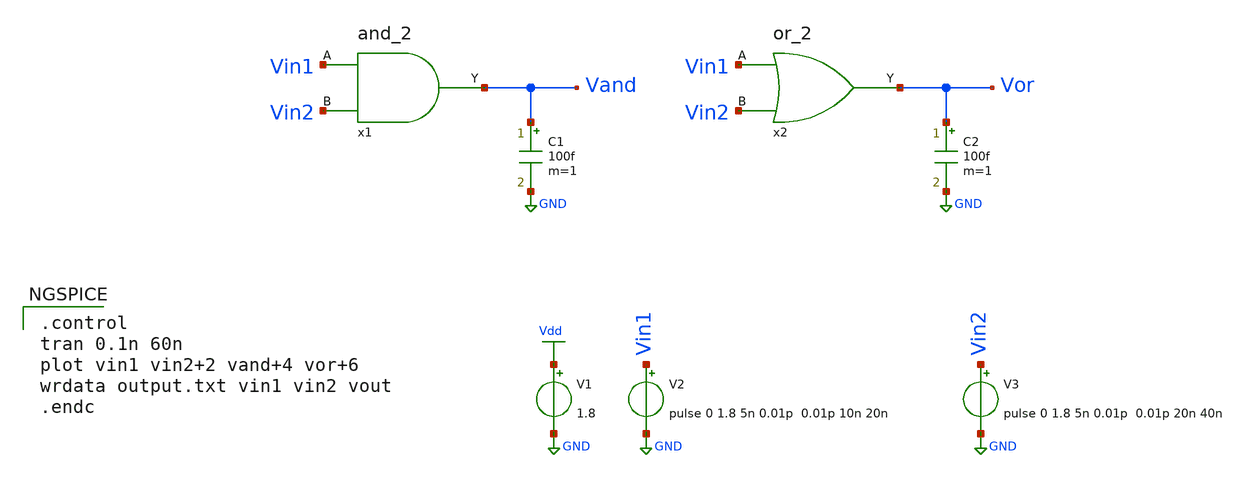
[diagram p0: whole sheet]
** sch_path: Circuiti/porta-nor.sch
**.subckt porta-nor
V1 Vdd GND 1.8
V2 Vin1 GND pulse 0 1.8 5n 0.01p 0.01p 10n 20n
C1 Vand GND 100f m=1
V3 Vin2 GND pulse 0 1.8 5n 0.01p 0.01p 20n 40n
x1 Vin1 Vand Vin2 and_2
C2 Vor GND 100f m=1
x2 Vin1 Vor Vin2 or_2
**** begin user architecture code


.lib /home/matteo/xschem_downloads/skywater-pdk/libraries/sky130_fd_pr_ngspice/latest/models/sky130.lib.spice tt

*.include /home/matteo/xschem_downloads/skywater-pdk/libraries/sky130_fd_pr_ngspice/latest/cells/nfet_01v8/sky130_fd_pr__nfet_01v8__tt.corner.spice

.param mc_mm_switch=0
.param mc_pr_switch=1



.control
tran 0.1n 60n
plot vin1 vin2+2 vand+4 vor+6
wrdata output.txt vin1 vin2 vout
.endc


**** end user architecture code
**.ends

* expanding   symbol:  /home/matteo/Documenti/tesi/Circuiti/logic_gates_sch_sym/and_2.sym # of
*+ pins=3
** sym_path: Circuiti/logic_gates_sch_sym/and_2.sym
** sch_path: Circuiti/logic_gates_sch_sym/and_2.sch
.subckt and_2 A Y B
*.ipin B
*.ipin A
*.opin Y
x1 A net1 B nand_2
x2 net1 Y not
.ends


* expanding   symbol:  /home/matteo/Documenti/tesi/Circuiti/logic_gates_sch_sym/or_2.sym # of pins=3
** sym_path: Circuiti/logic_gates_sch_sym/or_2.sym
** sch_path: Circuiti/logic_gates_sch_sym/or_2.sch
.subckt or_2 A Y B
*.ipin A
*.ipin B
*.opin Y
x1 A net1 B nor_2
x2 net1 Y not
.ends


* expanding   symbol:  /home/matteo/Documenti/tesi/Circuiti/logic_gates_sch_sym/nand_2.sym # of
*+ pins=3
** sym_path: Circuiti/logic_gates_sch_sym/nand_2.sym
** sch_path: Circuiti/logic_gates_sch_sym/nand_2.sch
.subckt nand_2 A Y B
*.ipin A
*.ipin B
*.opin Y
XM1 Y A net1 GND sky130_fd_pr__nfet_01v8 L=0.15 W=1 nf=1 ad='int((nf+1)/2) * W/nf * 0.29' as='int((nf+2)/2) * W/nf * 0.29'
+ pd='2*int((nf+1)/2) * (W/nf + 0.29)' ps='2*int((nf+2)/2) * (W/nf + 0.29)' nrd='0.29 / W' nrs='0.29 / W'
+ sa=0 sb=0 sd=0 mult=1 m=1
XM3 Y B Vdd VDD sky130_fd_pr__pfet_01v8 L=0.45 W=4.8 nf=1 ad='int((nf+1)/2) * W/nf * 0.29' as='int((nf+2)/2) * W/nf * 0.29'
+ pd='2*int((nf+1)/2) * (W/nf + 0.29)' ps='2*int((nf+2)/2) * (W/nf + 0.29)' nrd='0.29 / W' nrs='0.29 / W'
+ sa=0 sb=0 sd=0 mult=1 m=1
XM4 Y A Vdd VDD sky130_fd_pr__pfet_01v8 L=0.45 W=4.8 nf=1 ad='int((nf+1)/2) * W/nf * 0.29' as='int((nf+2)/2) * W/nf * 0.29'
+ pd='2*int((nf+1)/2) * (W/nf + 0.29)' ps='2*int((nf+2)/2) * (W/nf + 0.29)' nrd='0.29 / W' nrs='0.29 / W'
+ sa=0 sb=0 sd=0 mult=1 m=1
XM2 net1 B GND GND sky130_fd_pr__nfet_01v8 L=0.15 W=1 nf=1 ad='int((nf+1)/2) * W/nf * 0.29' as='int((nf+2)/2) * W/nf * 0.29'
+ pd='2*int((nf+1)/2) * (W/nf + 0.29)' ps='2*int((nf+2)/2) * (W/nf + 0.29)' nrd='0.29 / W' nrs='0.29 / W'
+ sa=0 sb=0 sd=0 mult=1 m=1
.ends


* expanding   symbol:  /home/matteo/Documenti/tesi/Circuiti/logic_gates_sch_sym/not.sym # of pins=2
** sym_path: Circuiti/logic_gates_sch_sym/not.sym
** sch_path: Circuiti/logic_gates_sch_sym/not.sch
.subckt not A Y
*.ipin A
*.opin Y
XM1 Y A GND GND sky130_fd_pr__nfet_01v8 L=0.45 W=1 nf=1 ad='int((nf+1)/2) * W/nf * 0.29' as='int((nf+2)/2) * W/nf * 0.29'
+ pd='2*int((nf+1)/2) * (W/nf + 0.29)' ps='2*int((nf+2)/2) * (W/nf + 0.29)' nrd='0.29 / W' nrs='0.29 / W'
+ sa=0 sb=0 sd=0 mult=1 m=1
XM2 Y A Vdd VDD sky130_fd_pr__pfet_01v8 L=0.45 W=4.8 nf=1 ad='int((nf+1)/2) * W/nf * 0.29' as='int((nf+2)/2) * W/nf * 0.29'
+ pd='2*int((nf+1)/2) * (W/nf + 0.29)' ps='2*int((nf+2)/2) * (W/nf + 0.29)' nrd='0.29 / W' nrs='0.29 / W'
+ sa=0 sb=0 sd=0 mult=1 m=1
.ends


* expanding   symbol:  /home/matteo/Documenti/tesi/Circuiti/logic_gates_sch_sym/nor_2.sym # of
*+ pins=3
** sym_path: Circuiti/logic_gates_sch_sym/nor_2.sym
** sch_path: Circuiti/logic_gates_sch_sym/nor_2.sch
.subckt nor_2 A Y B
*.opin Y
*.ipin A
*.ipin B
XM1 Y B GND GND sky130_fd_pr__nfet_01v8 L=0.45 W=1 nf=1 ad='int((nf+1)/2) * W/nf * 0.29' as='int((nf+2)/2) * W/nf * 0.29'
+ pd='2*int((nf+1)/2) * (W/nf + 0.29)' ps='2*int((nf+2)/2) * (W/nf + 0.29)' nrd='0.29 / W' nrs='0.29 / W'
+ sa=0 sb=0 sd=0 mult=1 m=1
XM3 Y B net1 VDD sky130_fd_pr__pfet_01v8 L=0.15 W=4.8 nf=1 ad='int((nf+1)/2) * W/nf * 0.29' as='int((nf+2)/2) * W/nf * 0.29'
+ pd='2*int((nf+1)/2) * (W/nf + 0.29)' ps='2*int((nf+2)/2) * (W/nf + 0.29)' nrd='0.29 / W' nrs='0.29 / W'
+ sa=0 sb=0 sd=0 mult=1 m=1
XM4 net1 A Vdd VDD sky130_fd_pr__pfet_01v8 L=0.15 W=4.8 nf=1 ad='int((nf+1)/2) * W/nf * 0.29' as='int((nf+2)/2) * W/nf * 0.29'
+ pd='2*int((nf+1)/2) * (W/nf + 0.29)' ps='2*int((nf+2)/2) * (W/nf + 0.29)' nrd='0.29 / W' nrs='0.29 / W'
+ sa=0 sb=0 sd=0 mult=1 m=1
XM2 Y A GND GND sky130_fd_pr__nfet_01v8 L=0.45 W=1 nf=1 ad='int((nf+1)/2) * W/nf * 0.29' as='int((nf+2)/2) * W/nf * 0.29'
+ pd='2*int((nf+1)/2) * (W/nf + 0.29)' ps='2*int((nf+2)/2) * (W/nf + 0.29)' nrd='0.29 / W' nrs='0.29 / W'
+ sa=0 sb=0 sd=0 mult=1 m=1
.ends

.GLOBAL Vdd
.GLOBAL GND
.end
